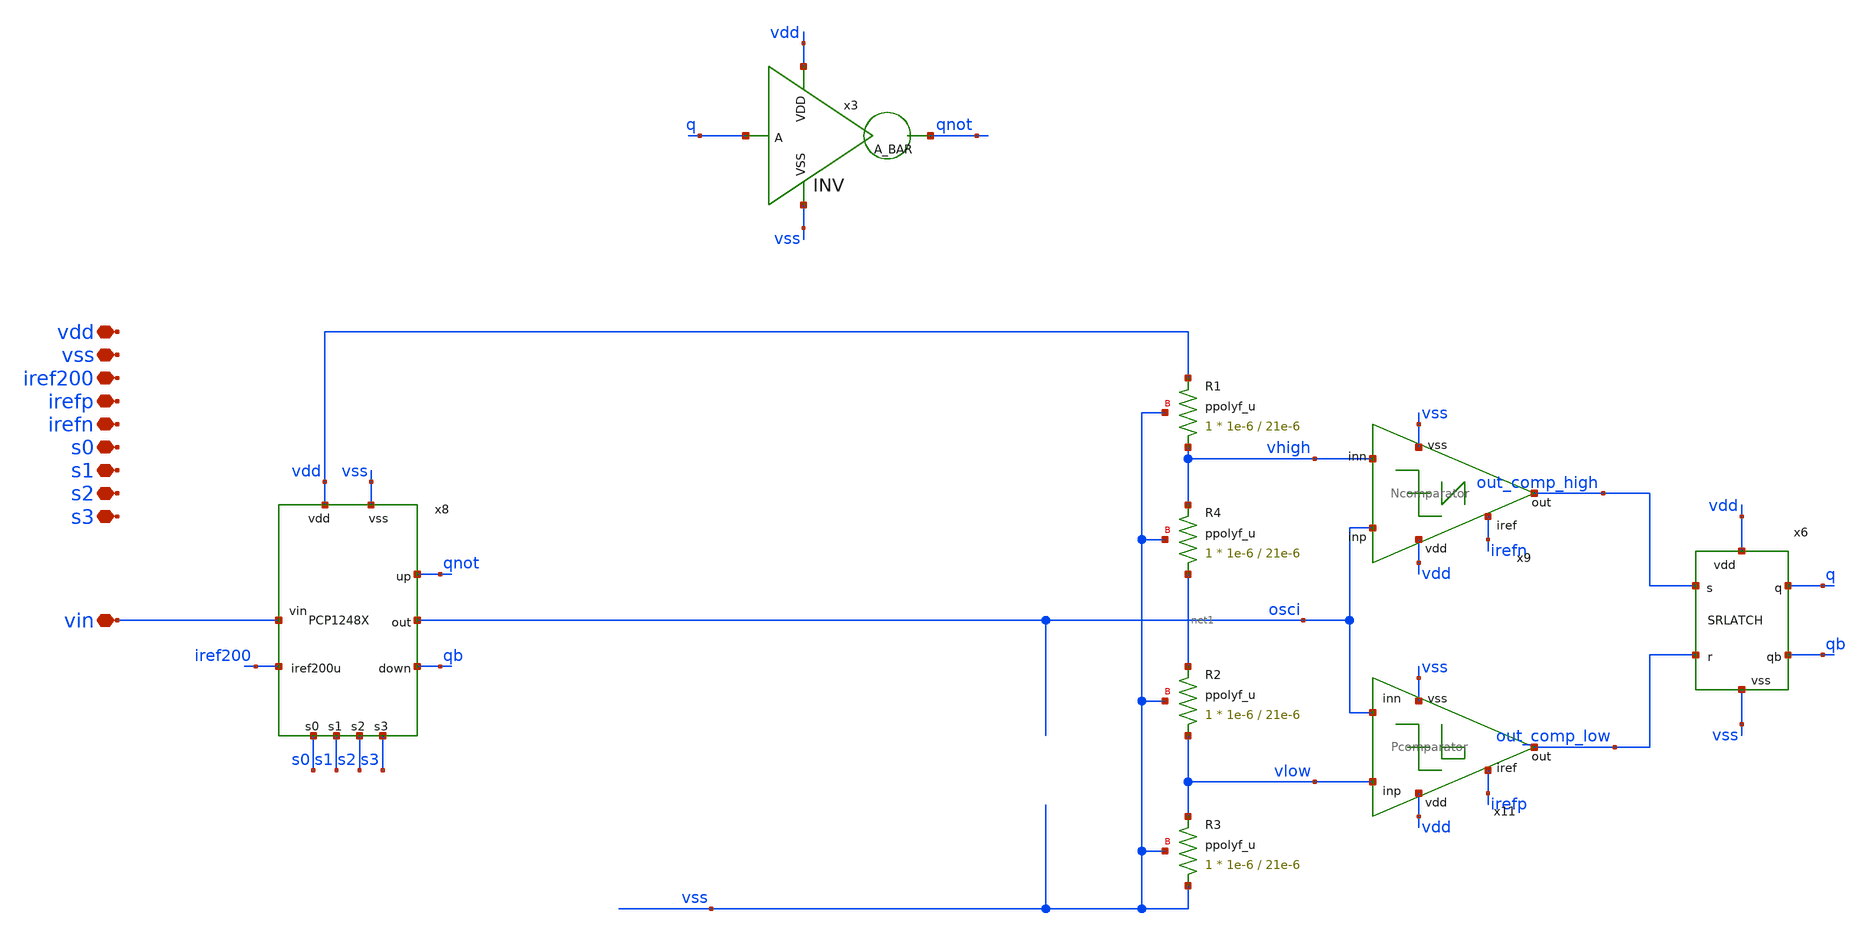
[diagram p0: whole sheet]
** sch_path: designs/libs/qw_core_analog/VCOfinal_flatten/VCOfinal_flatten.sch
**.subckt VCOfinal_flatten vin vdd vss iref200 irefp irefn s0 s1 s2 s3
*.iopin vin
*.iopin vdd
*.iopin vss
*.iopin iref200
*.iopin irefp
*.iopin irefn
*.iopin s0
*.iopin s1
*.iopin s2
*.iopin s3
x3 vdd q qnot vss INV
x8 vdd vss vin iref200 osci qnot qb s0 s1 s2 s3 PCP1248X
XR3 vss vlow vss ppolyf_u r_width=1e-6 r_length=21e-6 m=1
XR1 vhigh vdd vss ppolyf_u r_width=1e-6 r_length=21e-6 m=1
XR2 vlow net1 vss ppolyf_u r_width=1e-6 r_length=21e-6 m=1
XR4 net1 vhigh vss ppolyf_u r_width=1e-6 r_length=21e-6 m=1
x6 vdd out_comp_high q qb out_comp_low vss SRLATCH
x9 vdd osci out_comp_high vhigh irefn vss Ncomparator
x11 vdd irefp vlow out_comp_low osci vss Pcomparator
**.ends
.end
